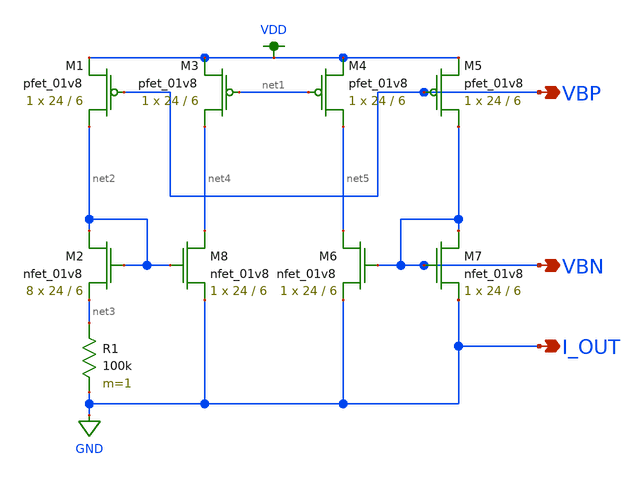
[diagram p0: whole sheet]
** sch_path: schemas/biasGen.sch
**.subckt biasGen VBN VBP I_OUT
*.opin VBN
*.opin VBP
*.opin I_OUT
XM1 net2 VBP VDD VDD sky130_fd_pr__pfet_01v8 L=6 W=24 nf=1 ad='int((nf+1)/2) * W/nf * 0.29' as='int((nf+2)/2) * W/nf * 0.29'
+ pd='2*int((nf+1)/2) * (W/nf + 0.29)' ps='2*int((nf+2)/2) * (W/nf + 0.29)' nrd='0.29 / W' nrs='0.29 / W'
+ sa=0 sb=0 sd=0 mult=1 m=1
XM2 net2 net2 net3 GND sky130_fd_pr__nfet_01v8 L=6 W=24 nf=1 ad='int((nf+1)/2) * W/nf * 0.29' as='int((nf+2)/2) * W/nf * 0.29'
+ pd='2*int((nf+1)/2) * (W/nf + 0.29)' ps='2*int((nf+2)/2) * (W/nf + 0.29)' nrd='0.29 / W' nrs='0.29 / W'
+ sa=0 sb=0 sd=0 mult=8 m=8
XM3 net4 net1 VDD VDD sky130_fd_pr__pfet_01v8 L=6 W=24 nf=1 ad='int((nf+1)/2) * W/nf * 0.29' as='int((nf+2)/2) * W/nf * 0.29'
+ pd='2*int((nf+1)/2) * (W/nf + 0.29)' ps='2*int((nf+2)/2) * (W/nf + 0.29)' nrd='0.29 / W' nrs='0.29 / W'
+ sa=0 sb=0 sd=0 mult=1 m=1
XM4 net5 net1 VDD VDD sky130_fd_pr__pfet_01v8 L=6 W=24 nf=1 ad='int((nf+1)/2) * W/nf * 0.29' as='int((nf+2)/2) * W/nf * 0.29'
+ pd='2*int((nf+1)/2) * (W/nf + 0.29)' ps='2*int((nf+2)/2) * (W/nf + 0.29)' nrd='0.29 / W' nrs='0.29 / W'
+ sa=0 sb=0 sd=0 mult=1 m=1
XM5 VBN VBP VDD VDD sky130_fd_pr__pfet_01v8 L=6 W=24 nf=1 ad='int((nf+1)/2) * W/nf * 0.29' as='int((nf+2)/2) * W/nf * 0.29'
+ pd='2*int((nf+1)/2) * (W/nf + 0.29)' ps='2*int((nf+2)/2) * (W/nf + 0.29)' nrd='0.29 / W' nrs='0.29 / W'
+ sa=0 sb=0 sd=0 mult=1 m=1
XM6 net5 VBN GND GND sky130_fd_pr__nfet_01v8 L=6 W=24 nf=1 ad='int((nf+1)/2) * W/nf * 0.29' as='int((nf+2)/2) * W/nf * 0.29'
+ pd='2*int((nf+1)/2) * (W/nf + 0.29)' ps='2*int((nf+2)/2) * (W/nf + 0.29)' nrd='0.29 / W' nrs='0.29 / W'
+ sa=0 sb=0 sd=0 mult=1 m=1
XM7 VBN VBN GND GND sky130_fd_pr__nfet_01v8 L=6 W=24 nf=1 ad='int((nf+1)/2) * W/nf * 0.29' as='int((nf+2)/2) * W/nf * 0.29'
+ pd='2*int((nf+1)/2) * (W/nf + 0.29)' ps='2*int((nf+2)/2) * (W/nf + 0.29)' nrd='0.29 / W' nrs='0.29 / W'
+ sa=0 sb=0 sd=0 mult=1 m=1
XM8 net4 net2 GND GND sky130_fd_pr__nfet_01v8 L=6 W=24 nf=1 ad='int((nf+1)/2) * W/nf * 0.29' as='int((nf+2)/2) * W/nf * 0.29'
+ pd='2*int((nf+1)/2) * (W/nf + 0.29)' ps='2*int((nf+2)/2) * (W/nf + 0.29)' nrd='0.29 / W' nrs='0.29 / W'
+ sa=0 sb=0 sd=0 mult=1 m=1
R1 net3 GND 100k m=1
**.ends
.GLOBAL GND
.GLOBAL VDD
.end
